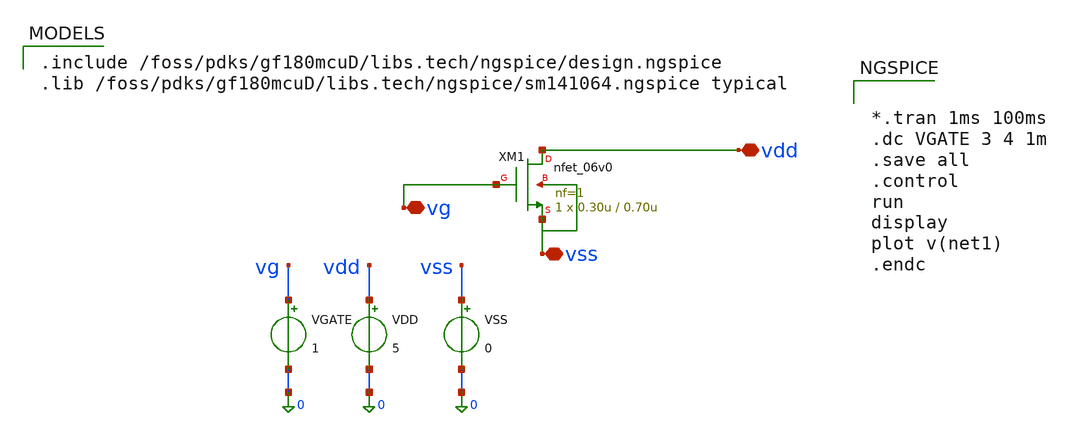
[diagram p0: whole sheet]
** sch_path: activities/opamp3An/NMOSresistor_tb.sch
**.subckt NMOSresistor_tb
VGATE vg 0 1
VDD vdd 0 5
VSS vss 0 0
**** begin user architecture code

.include /foss/pdks/gf180mcuD/libs.tech/ngspice/design.ngspice
.lib /foss/pdks/gf180mcuD/libs.tech/ngspice/sm141064.ngspice typical



*.tran 1ms 100ms
.dc VGATE 3 4 1m
.save all
.control
run
display
plot v(net1)
.endc


**** end user architecture code
**.ends
.end
